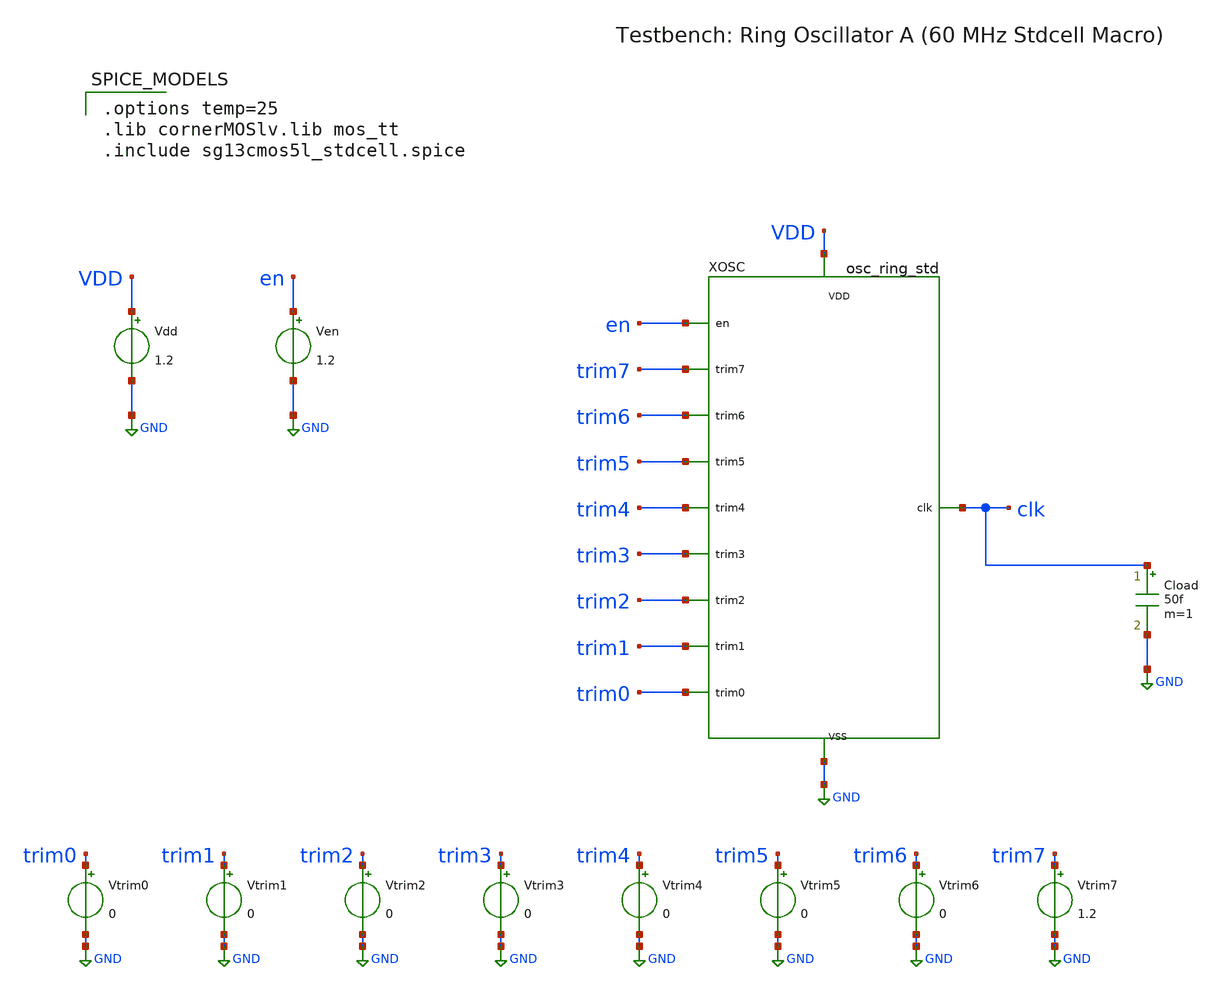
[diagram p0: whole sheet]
** sch_path: analog/osc_ring_std/tb_osc_ring_std.sch
**.subckt tb_osc_ring_std
XOSC VDD GND en trim7 trim6 trim5 trim4 trim3 trim2 trim1 trim0 clk osc_ring_std
Vdd VDD GND 1.2
Ven en GND 1.2
Vtrim0 trim0 GND 0
Vtrim1 trim1 GND 0
Vtrim2 trim2 GND 0
Vtrim3 trim3 GND 0
Vtrim4 trim4 GND 0
Vtrim5 trim5 GND 0
Vtrim6 trim6 GND 0
Vtrim7 trim7 GND 1.2
Cload clk GND 50f m=1
**** begin user architecture code

.options temp=25
.lib cornerMOSlv.lib mos_tt
.include sg13cmos5l_stdcell.spice


**** end user architecture code
**.ends

* expanding   symbol:  osc_ring_std/osc_ring_std.sym # of pins=12
** sym_path: analog/osc_ring_std/osc_ring_std.sym
** sch_path: analog/osc_ring_std/osc_ring_std.sch
.subckt osc_ring_std VDD VSS en trim7 trim6 trim5 trim4 trim3 trim2 trim1 trim0 clk
*.iopin VDD
*.iopin VSS
*.ipin en
*.ipin trim7
*.ipin trim6
*.ipin trim5
*.ipin trim4
*.ipin trim3
*.ipin trim2
*.ipin trim1
*.ipin trim0
*.opin clk
XNAND n_nand loop_fb en VDD VSS sg13cmos5l_nand2_2
XOUT_INV net1 n_nand VDD VSS sg13cmos5l_inv_2
XOUT_BUF clk net1 VDD VSS sg13cmos5l_buf_4
XFIX0 net2 n_nand VDD VSS sg13cmos5l_dlygate4sd3_1
XFIX1 net3 net2 VDD VSS sg13cmos5l_dlygate4sd3_1
XFIX2 net4 net3 VDD VSS sg13cmos5l_dlygate4sd3_1
XFIX3 net5 net4 VDD VSS sg13cmos5l_dlygate4sd3_1
XFIX4 net6 net5 VDD VSS sg13cmos5l_dlygate4sd3_1
XFIX5 net7 net6 VDD VSS sg13cmos5l_dlygate4sd3_1
XFIX6 net8 net7 VDD VSS sg13cmos5l_dlygate4sd3_1
XFIX7 fix_out net8 VDD VSS sg13cmos5l_dlygate4sd3_1
XFINE_SLOW net9 fix_out VDD VSS sg13cmos5l_dlygate4sd1_1
XFINE_FAST net10 fix_out VDD VSS sg13cmos5l_buf_1
XMUX_FINE chain_0 net9 net10 trim0 VDD VSS sg13cmos5l_mux2_1
XSLICE7 VDD VSS chain_0 trim4 trim3 trim2 trim1 chain_1 smux_7 tap_chain_16
XSLICE6 VDD VSS chain_1 trim4 trim3 trim2 trim1 chain_2 smux_6 tap_chain_16
XSLICE5 VDD VSS chain_2 trim4 trim3 trim2 trim1 chain_3 smux_5 tap_chain_16
XSLICE4 VDD VSS chain_3 trim4 trim3 trim2 trim1 chain_4 smux_4 tap_chain_16
XSLICE3 VDD VSS chain_4 trim4 trim3 trim2 trim1 chain_5 smux_3 tap_chain_16
XSLICE2 VDD VSS chain_5 trim4 trim3 trim2 trim1 chain_6 smux_2 tap_chain_16
XSLICE1 VDD VSS chain_6 trim4 trim3 trim2 trim1 chain_7 smux_1 tap_chain_16
XSLICE0 VDD VSS chain_7 trim4 trim3 trim2 trim1 chain_end smux_0 tap_chain_16
* noconn chain_end
XFM0_0 net11 smux_0 smux_1 trim5 VDD VSS sg13cmos5l_mux2_1
XFM0_1 net12 smux_2 smux_3 trim5 VDD VSS sg13cmos5l_mux2_1
XFM0_2 net13 smux_4 smux_5 trim5 VDD VSS sg13cmos5l_mux2_1
XFM0_3 net14 smux_6 smux_7 trim5 VDD VSS sg13cmos5l_mux2_1
XFM1_0 net15 net11 net12 trim6 VDD VSS sg13cmos5l_mux2_1
XFM1_1 net16 net13 net14 trim6 VDD VSS sg13cmos5l_mux2_1
XFM2_0 loop_fb net15 net16 trim7 VDD VSS sg13cmos5l_mux2_1
.ends


* expanding   symbol:  osc_ring_std/tap_chain_16.sym # of pins=9
** sym_path: analog/osc_ring_std/tap_chain_16.sym
** sch_path: analog/osc_ring_std/tap_chain_16.sch
.subckt tap_chain_16 VDD VSS in s3 s2 s1 s0 out_chain out_mux
*.iopin VDD
*.iopin VSS
*.ipin in
*.ipin s3
*.ipin s2
*.ipin s1
*.ipin s0
*.opin out_chain
*.opin out_mux
XDLY0 t1 in VDD VSS sg13cmos5l_dlygate4sd1_1
XDLY1 t2 t1 VDD VSS sg13cmos5l_dlygate4sd1_1
XDLY2 t3 t2 VDD VSS sg13cmos5l_dlygate4sd1_1
XDLY3 t4 t3 VDD VSS sg13cmos5l_dlygate4sd1_1
XDLY4 t5 t4 VDD VSS sg13cmos5l_dlygate4sd1_1
XDLY5 t6 t5 VDD VSS sg13cmos5l_dlygate4sd1_1
XDLY6 t7 t6 VDD VSS sg13cmos5l_dlygate4sd1_1
XDLY7 t8 t7 VDD VSS sg13cmos5l_dlygate4sd1_1
XDLY8 t9 t8 VDD VSS sg13cmos5l_dlygate4sd1_1
XDLY9 t10 t9 VDD VSS sg13cmos5l_dlygate4sd1_1
XDLY10 t11 t10 VDD VSS sg13cmos5l_dlygate4sd1_1
XDLY11 t12 t11 VDD VSS sg13cmos5l_dlygate4sd1_1
XDLY12 t13 t12 VDD VSS sg13cmos5l_dlygate4sd1_1
XDLY13 t14 t13 VDD VSS sg13cmos5l_dlygate4sd1_1
XDLY14 t15 t14 VDD VSS sg13cmos5l_dlygate4sd1_1
XDLY15 out_chain t15 VDD VSS sg13cmos5l_dlygate4sd1_1
XM0_0 net1 t15 t14 s0 VDD VSS sg13cmos5l_mux2_1
XM0_1 net2 t13 t12 s0 VDD VSS sg13cmos5l_mux2_1
XM0_2 net3 t11 t10 s0 VDD VSS sg13cmos5l_mux2_1
XM0_3 net4 t9 t8 s0 VDD VSS sg13cmos5l_mux2_1
XM0_4 net5 t7 t6 s0 VDD VSS sg13cmos5l_mux2_1
XM0_5 net6 t5 t4 s0 VDD VSS sg13cmos5l_mux2_1
XM0_6 net7 t3 t2 s0 VDD VSS sg13cmos5l_mux2_1
XM0_7 net8 t1 in s0 VDD VSS sg13cmos5l_mux2_1
XM1_0 net9 net1 net2 s1 VDD VSS sg13cmos5l_mux2_1
XM1_1 net10 net3 net4 s1 VDD VSS sg13cmos5l_mux2_1
XM1_2 net11 net5 net6 s1 VDD VSS sg13cmos5l_mux2_1
XM1_3 net12 net7 net8 s1 VDD VSS sg13cmos5l_mux2_1
XM2_0 net13 net9 net10 s2 VDD VSS sg13cmos5l_mux2_1
XM2_1 net14 net11 net12 s2 VDD VSS sg13cmos5l_mux2_1
XM3_0 out_mux net13 net14 s3 VDD VSS sg13cmos5l_mux2_1
.ends

.GLOBAL GND
.end
